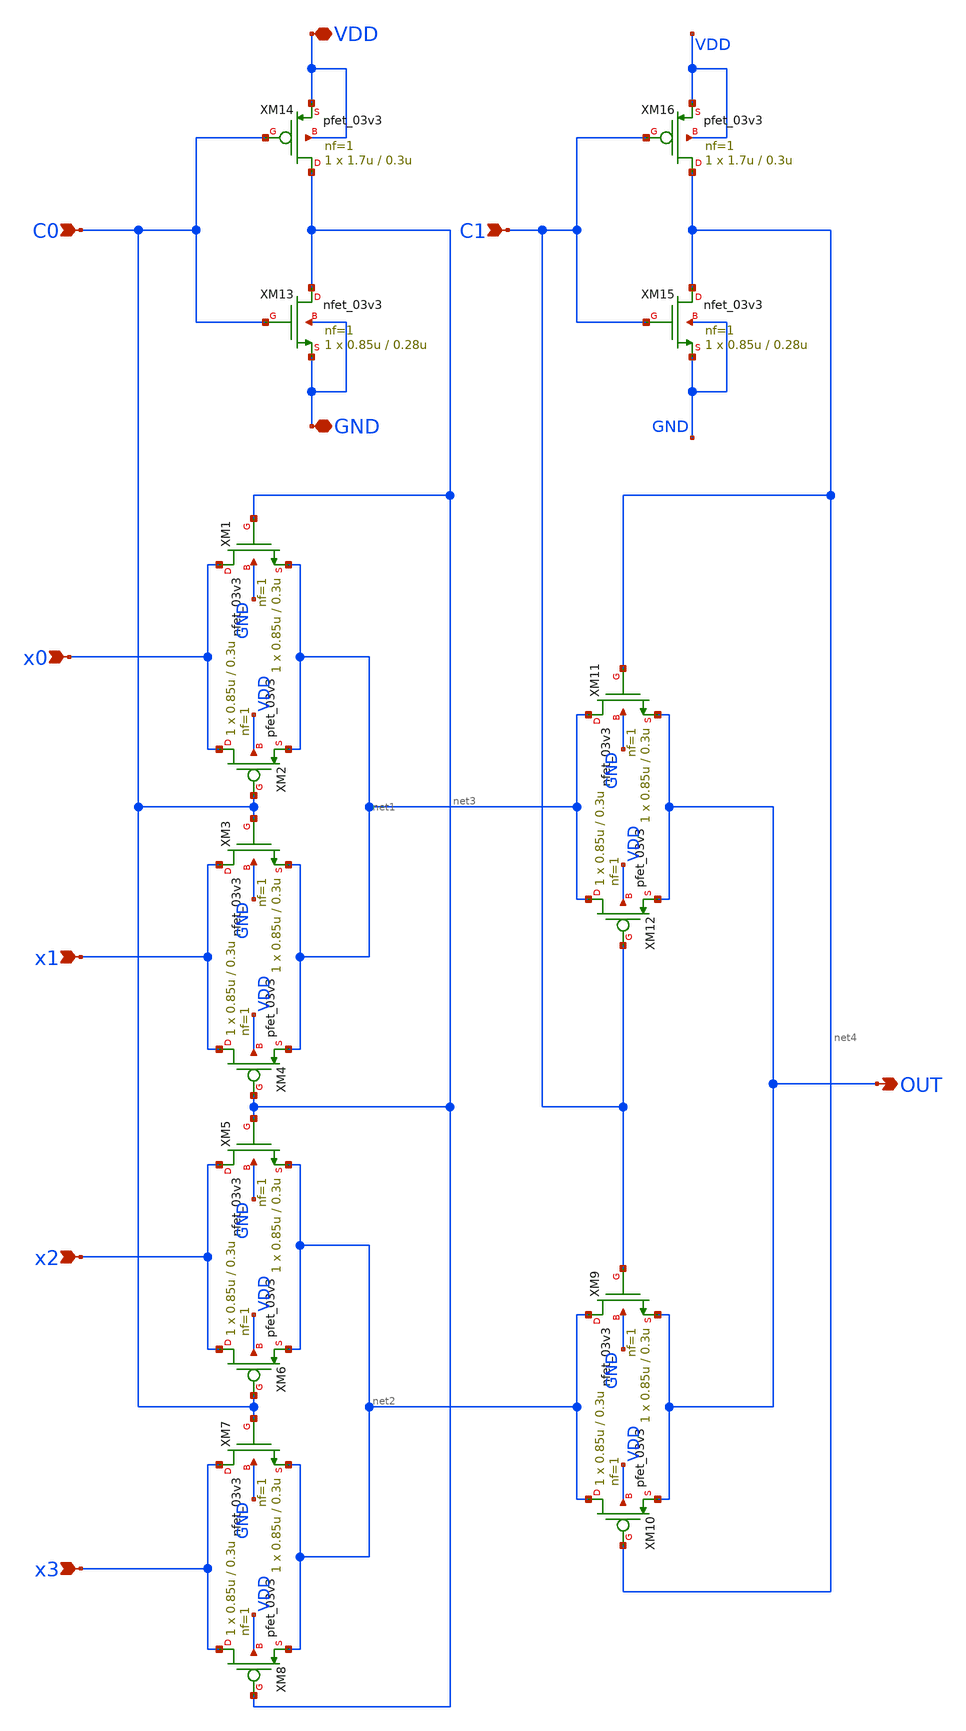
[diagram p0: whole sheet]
** sch_path: designs/schematic/MUX4/mux4.sch
**.subckt mux4 x0 x1 x2 x3 C0 C1 OUT VDD GND
*.ipin x0
*.ipin x1
*.ipin x2
*.ipin x3
*.ipin C0
*.ipin C1
*.opin OUT
*.iopin VDD
*.iopin GND
XM1 x0 net3 net1 GND nfet_03v3 L=0.3u W=0.85u nf=1 ad='int((nf+1)/2) * W/nf * 0.18u' as='int((nf+2)/2) * W/nf * 0.18u'
+ pd='2*int((nf+1)/2) * (W/nf + 0.18u)' ps='2*int((nf+2)/2) * (W/nf + 0.18u)' nrd='0.18u / W' nrs='0.18u / W'
+ sa=0 sb=0 sd=0 m=1
XM2 x0 C0 net1 VDD pfet_03v3 L=0.3u W=0.85u nf=1 ad='int((nf+1)/2) * W/nf * 0.18u' as='int((nf+2)/2) * W/nf * 0.18u'
+ pd='2*int((nf+1)/2) * (W/nf + 0.18u)' ps='2*int((nf+2)/2) * (W/nf + 0.18u)' nrd='0.18u / W' nrs='0.18u / W'
+ sa=0 sb=0 sd=0 m=1
XM3 x1 C0 net1 GND nfet_03v3 L=0.3u W=0.85u nf=1 ad='int((nf+1)/2) * W/nf * 0.18u' as='int((nf+2)/2) * W/nf * 0.18u'
+ pd='2*int((nf+1)/2) * (W/nf + 0.18u)' ps='2*int((nf+2)/2) * (W/nf + 0.18u)' nrd='0.18u / W' nrs='0.18u / W'
+ sa=0 sb=0 sd=0 m=1
XM5 x2 net3 net2 GND nfet_03v3 L=0.3u W=0.85u nf=1 ad='int((nf+1)/2) * W/nf * 0.18u' as='int((nf+2)/2) * W/nf * 0.18u'
+ pd='2*int((nf+1)/2) * (W/nf + 0.18u)' ps='2*int((nf+2)/2) * (W/nf + 0.18u)' nrd='0.18u / W' nrs='0.18u / W'
+ sa=0 sb=0 sd=0 m=1
XM7 x3 C0 net2 GND nfet_03v3 L=0.3u W=0.85u nf=1 ad='int((nf+1)/2) * W/nf * 0.18u' as='int((nf+2)/2) * W/nf * 0.18u'
+ pd='2*int((nf+1)/2) * (W/nf + 0.18u)' ps='2*int((nf+2)/2) * (W/nf + 0.18u)' nrd='0.18u / W' nrs='0.18u / W'
+ sa=0 sb=0 sd=0 m=1
XM9 net2 C1 OUT GND nfet_03v3 L=0.3u W=0.85u nf=1 ad='int((nf+1)/2) * W/nf * 0.18u' as='int((nf+2)/2) * W/nf * 0.18u'
+ pd='2*int((nf+1)/2) * (W/nf + 0.18u)' ps='2*int((nf+2)/2) * (W/nf + 0.18u)' nrd='0.18u / W' nrs='0.18u / W'
+ sa=0 sb=0 sd=0 m=1
XM11 net1 net4 OUT GND nfet_03v3 L=0.3u W=0.85u nf=1 ad='int((nf+1)/2) * W/nf * 0.18u' as='int((nf+2)/2) * W/nf * 0.18u'
+ pd='2*int((nf+1)/2) * (W/nf + 0.18u)' ps='2*int((nf+2)/2) * (W/nf + 0.18u)' nrd='0.18u / W' nrs='0.18u / W'
+ sa=0 sb=0 sd=0 m=1
XM4 x1 net3 net1 VDD pfet_03v3 L=0.3u W=0.85u nf=1 ad='int((nf+1)/2) * W/nf * 0.18u' as='int((nf+2)/2) * W/nf * 0.18u'
+ pd='2*int((nf+1)/2) * (W/nf + 0.18u)' ps='2*int((nf+2)/2) * (W/nf + 0.18u)' nrd='0.18u / W' nrs='0.18u / W'
+ sa=0 sb=0 sd=0 m=1
XM6 x2 C0 net2 VDD pfet_03v3 L=0.3u W=0.85u nf=1 ad='int((nf+1)/2) * W/nf * 0.18u' as='int((nf+2)/2) * W/nf * 0.18u'
+ pd='2*int((nf+1)/2) * (W/nf + 0.18u)' ps='2*int((nf+2)/2) * (W/nf + 0.18u)' nrd='0.18u / W' nrs='0.18u / W'
+ sa=0 sb=0 sd=0 m=1
XM8 x3 net3 net2 VDD pfet_03v3 L=0.3u W=0.85u nf=1 ad='int((nf+1)/2) * W/nf * 0.18u' as='int((nf+2)/2) * W/nf * 0.18u'
+ pd='2*int((nf+1)/2) * (W/nf + 0.18u)' ps='2*int((nf+2)/2) * (W/nf + 0.18u)' nrd='0.18u / W' nrs='0.18u / W'
+ sa=0 sb=0 sd=0 m=1
XM10 net2 net4 OUT VDD pfet_03v3 L=0.3u W=0.85u nf=1 ad='int((nf+1)/2) * W/nf * 0.18u' as='int((nf+2)/2) * W/nf * 0.18u'
+ pd='2*int((nf+1)/2) * (W/nf + 0.18u)' ps='2*int((nf+2)/2) * (W/nf + 0.18u)' nrd='0.18u / W' nrs='0.18u / W'
+ sa=0 sb=0 sd=0 m=1
XM12 net1 C1 OUT VDD pfet_03v3 L=0.3u W=0.85u nf=1 ad='int((nf+1)/2) * W/nf * 0.18u' as='int((nf+2)/2) * W/nf * 0.18u'
+ pd='2*int((nf+1)/2) * (W/nf + 0.18u)' ps='2*int((nf+2)/2) * (W/nf + 0.18u)' nrd='0.18u / W' nrs='0.18u / W'
+ sa=0 sb=0 sd=0 m=1
XM13 net3 C0 GND GND nfet_03v3 L=0.28u W=0.85u nf=1 ad='int((nf+1)/2) * W/nf * 0.18u' as='int((nf+2)/2) * W/nf * 0.18u'
+ pd='2*int((nf+1)/2) * (W/nf + 0.18u)' ps='2*int((nf+2)/2) * (W/nf + 0.18u)' nrd='0.18u / W' nrs='0.18u / W'
+ sa=0 sb=0 sd=0 m=1
XM14 net3 C0 VDD VDD pfet_03v3 L=0.3u W=1.7u nf=1 ad='int((nf+1)/2) * W/nf * 0.18u' as='int((nf+2)/2) * W/nf * 0.18u'
+ pd='2*int((nf+1)/2) * (W/nf + 0.18u)' ps='2*int((nf+2)/2) * (W/nf + 0.18u)' nrd='0.18u / W' nrs='0.18u / W'
+ sa=0 sb=0 sd=0 m=1
XM15 net4 C1 GND GND nfet_03v3 L=0.28u W=0.85u nf=1 ad='int((nf+1)/2) * W/nf * 0.18u' as='int((nf+2)/2) * W/nf * 0.18u'
+ pd='2*int((nf+1)/2) * (W/nf + 0.18u)' ps='2*int((nf+2)/2) * (W/nf + 0.18u)' nrd='0.18u / W' nrs='0.18u / W'
+ sa=0 sb=0 sd=0 m=1
XM16 net4 C1 VDD VDD pfet_03v3 L=0.3u W=1.7u nf=1 ad='int((nf+1)/2) * W/nf * 0.18u' as='int((nf+2)/2) * W/nf * 0.18u'
+ pd='2*int((nf+1)/2) * (W/nf + 0.18u)' ps='2*int((nf+2)/2) * (W/nf + 0.18u)' nrd='0.18u / W' nrs='0.18u / W'
+ sa=0 sb=0 sd=0 m=1
**.ends
.end
